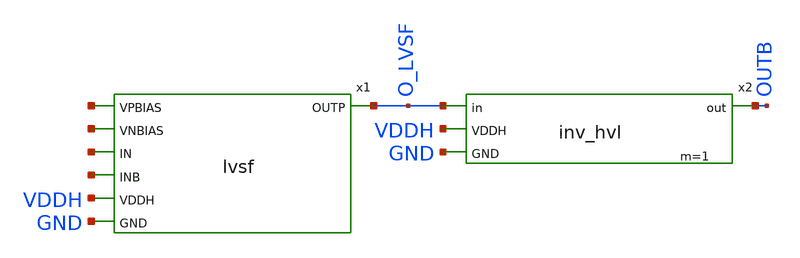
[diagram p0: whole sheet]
** sch_path: xschem/lvsf_1inv.sch
**.subckt lvsf_1inv
x1 net1 net2 net3 net4 O_LVSF VDDH GND lvsf
x2 O_LVSF OUTB VDDH GND inv_hvl m=1
**.ends

* expanding   symbol:  lvsf.sym # of pins=7
** sym_path: xschem/lvsf.sym
** sch_path: xschem/lvsf.sch
.subckt lvsf VPBIAS VNBIAS IN INB OUTP VDDH GND
*.ipin IN
*.ipin INB
*.opin OUTP
*.ipin VDDH
*.ipin GND
*.ipin VPBIAS
*.ipin VNBIAS
Vmeas net1 net2 0
.save i(vmeas)
XM13 net6 IN GND GND sky130_fd_pr__nfet_01v8 L=0.15 W=3 nf=1 ad='int((nf+1)/2) * W/nf * 0.29' as='int((nf+2)/2) * W/nf * 0.29'
+ pd='2*int((nf+1)/2) * (W/nf + 0.29)' ps='2*int((nf+2)/2) * (W/nf + 0.29)' nrd='0.29 / W' nrs='0.29 / W'
+ sa=0 sb=0 sd=0 mult=1 m=1
XM1 net3 VPBIAS VDDH VDDH sky130_fd_pr__pfet_g5v0d10v5 L=0.8 W=1 nf=1 ad='int((nf+1)/2) * W/nf * 0.29'
+ as='int((nf+2)/2) * W/nf * 0.29' pd='2*int((nf+1)/2) * (W/nf + 0.29)' ps='2*int((nf+2)/2) * (W/nf + 0.29)'
+ nrd='0.29 / W' nrs='0.29 / W' sa=0 sb=0 sd=0 mult=1 m=1
XM2 net1 VPBIAS VDDH VDDH sky130_fd_pr__pfet_g5v0d10v5 L=0.8 W=1 nf=1 ad='int((nf+1)/2) * W/nf * 0.29'
+ as='int((nf+2)/2) * W/nf * 0.29' pd='2*int((nf+1)/2) * (W/nf + 0.29)' ps='2*int((nf+2)/2) * (W/nf + 0.29)'
+ nrd='0.29 / W' nrs='0.29 / W' sa=0 sb=0 sd=0 mult=1 m=1
XM3 OUTPB OUTP net4 VDDH sky130_fd_pr__pfet_g5v0d10v5 L=0.8 W=1 nf=1 ad='int((nf+1)/2) * W/nf * 0.29'
+ as='int((nf+2)/2) * W/nf * 0.29' pd='2*int((nf+1)/2) * (W/nf + 0.29)' ps='2*int((nf+2)/2) * (W/nf + 0.29)'
+ nrd='0.29 / W' nrs='0.29 / W' sa=0 sb=0 sd=0 mult=1 m=1
XM4 OUTP OUTPB net2 VDDH sky130_fd_pr__pfet_g5v0d10v5 L=0.8 W=1 nf=1 ad='int((nf+1)/2) * W/nf * 0.29'
+ as='int((nf+2)/2) * W/nf * 0.29' pd='2*int((nf+1)/2) * (W/nf + 0.29)' ps='2*int((nf+2)/2) * (W/nf + 0.29)'
+ nrd='0.29 / W' nrs='0.29 / W' sa=0 sb=0 sd=0 mult=1 m=1
XM5 OUTPB VNBIAS n1 GND sky130_fd_pr__nfet_g5v0d10v5 L=1 W=1 nf=1 ad='int((nf+1)/2) * W/nf * 0.29' as='int((nf+2)/2) * W/nf * 0.29'
+ pd='2*int((nf+1)/2) * (W/nf + 0.29)' ps='2*int((nf+2)/2) * (W/nf + 0.29)' nrd='0.29 / W' nrs='0.29 / W'
+ sa=0 sb=0 sd=0 mult=1 m=1
XM6 OUTP VNBIAS n2 GND sky130_fd_pr__nfet_g5v0d10v5 L=1 W=1 nf=1 ad='int((nf+1)/2) * W/nf * 0.29' as='int((nf+2)/2) * W/nf * 0.29'
+ pd='2*int((nf+1)/2) * (W/nf + 0.29)' ps='2*int((nf+2)/2) * (W/nf + 0.29)' nrd='0.29 / W' nrs='0.29 / W'
+ sa=0 sb=0 sd=0 mult=1 m=1
Vmeas1 net3 net4 0
.save i(vmeas1)
XM7 net5 INB GND GND sky130_fd_pr__nfet_01v8 L=0.15 W=3 nf=1 ad='int((nf+1)/2) * W/nf * 0.29' as='int((nf+2)/2) * W/nf * 0.29'
+ pd='2*int((nf+1)/2) * (W/nf + 0.29)' ps='2*int((nf+2)/2) * (W/nf + 0.29)' nrd='0.29 / W' nrs='0.29 / W'
+ sa=0 sb=0 sd=0 mult=1 m=1
Vmeas2 n2 net5 0
.save i(vmeas2)
Vmeas3 n1 net6 0
.save i(vmeas3)
.ends


* expanding   symbol:  inv_hvl.sym # of pins=4
** sym_path: xschem/inv_hvl.sym
** sch_path: xschem/inv_hvl.sch
.subckt inv_hvl in out VDDH GND
*.opin out
*.ipin VDDH
*.ipin GND
*.ipin in
.param wp=0.84 wn=0.42 l=0.5
XM1 out in VDDH VDDH sky130_fd_pr__pfet_g5v0d10v5 L=l W=wp nf=1 ad='int((nf+1)/2) * W/nf * 0.29' as='int((nf+2)/2) * W/nf * 0.29'
+ pd='2*int((nf+1)/2) * (W/nf + 0.29)' ps='2*int((nf+2)/2) * (W/nf + 0.29)' nrd='0.29 / W' nrs='0.29 / W'
+ sa=0 sb=0 sd=0 mult=m m=m
XM2 out in GND GND sky130_fd_pr__nfet_g5v0d10v5 L=l W=wn nf=1 ad='int((nf+1)/2) * W/nf * 0.29' as='int((nf+2)/2) * W/nf * 0.29'
+ pd='2*int((nf+1)/2) * (W/nf + 0.29)' ps='2*int((nf+2)/2) * (W/nf + 0.29)' nrd='0.29 / W' nrs='0.29 / W'
+ sa=0 sb=0 sd=0 mult=m m=m
.ends

.end
